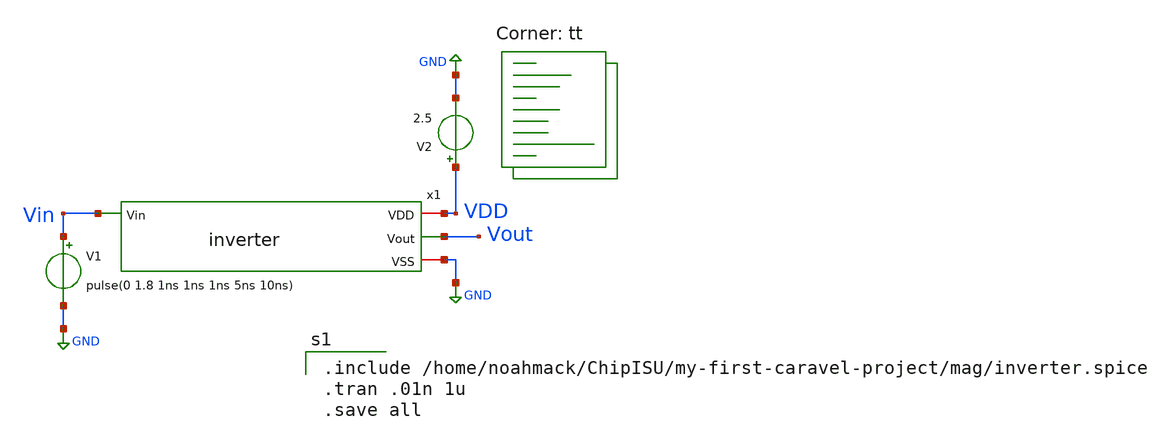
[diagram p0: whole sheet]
** sch_path: xschem/invTB_post.sch
**.subckt invTB_post
x1 VDD Vout Vin GND inverter
V1 Vin GND pulse(0 1.8 1ns 1ns 1ns 5ns 10ns)
V2 VDD GND 2.5
**** begin user architecture code
.lib $::SKYWATER_MODELS/sky130.lib.spice tt

.include /home/noahmack/ChipISU/my-first-caravel-project/mag/inverter.spice
.tran .01n 1u
.save all

**** end user architecture code
**.ends

* expanding   symbol:  inverter.sym # of pins=4
** sym_path: xschem/inverter.sym
** sch_path: xschem/inverter.sch
.subckt inverter VDD Vout Vin VSS
*.opin Vout
*.ipin Vin
*.iopin VSS
*.iopin VDD
XM3 Vout Vin VDD VDD sky130_fd_pr__pfet_g5v0d10v5 L=0.5 W=1 nf=1 ad='int((nf+1)/2) * W/nf * 0.29' as='int((nf+2)/2) * W/nf * 0.29'
+ pd='2*int((nf+1)/2) * (W/nf + 0.29)' ps='2*int((nf+2)/2) * (W/nf + 0.29)' nrd='0.29 / W' nrs='0.29 / W'
+ sa=0 sb=0 sd=0 mult=1 m=1
XM1 Vout Vin VSS VSS sky130_fd_pr__nfet_g5v0d10v5 L=0.5 W=1 nf=1 ad='int((nf+1)/2) * W/nf * 0.29' as='int((nf+2)/2) * W/nf * 0.29'
+ pd='2*int((nf+1)/2) * (W/nf + 0.29)' ps='2*int((nf+2)/2) * (W/nf + 0.29)' nrd='0.29 / W' nrs='0.29 / W'
+ sa=0 sb=0 sd=0 mult=1 m=1
.ends

.GLOBAL GND
.end
